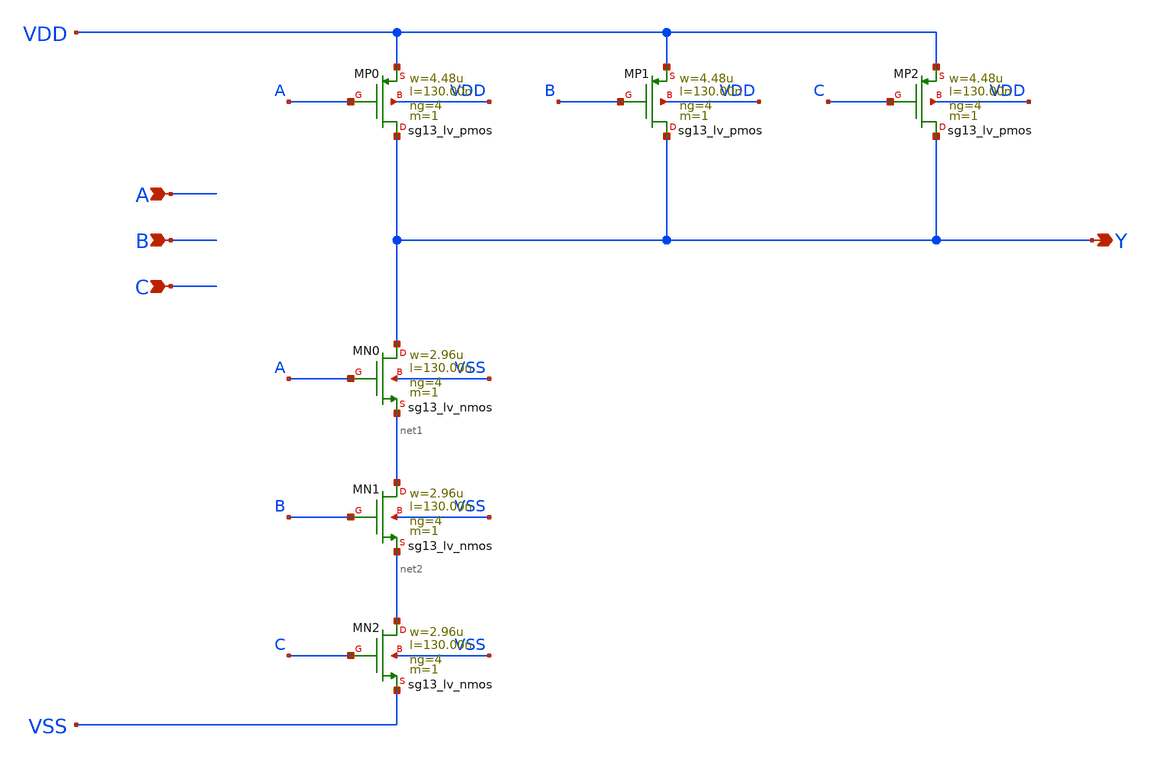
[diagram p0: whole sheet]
** sch_path: outputs/sg13g2_cells/cells/sg13g2_nand3_4/sg13g2_nand3_4.sch
**.subckt sg13g2_nand3_4 A B C Y
*.ipin A
*.ipin B
*.ipin C
*.opin Y
XMN1 net1 B net2 VSS sg13_lv_nmos w=2.96u l=130.00n ng=4 m=1 mm_ok=1
XMN2 net2 C VSS VSS sg13_lv_nmos w=2.96u l=130.00n ng=4 m=1 mm_ok=1
XMN0 Y A net1 VSS sg13_lv_nmos w=2.96u l=130.00n ng=4 m=1 mm_ok=1
XMP0 Y A VDD VDD sg13_lv_pmos w=4.48u l=130.00n ng=4 m=1 mm_ok=1
XMP1 Y B VDD VDD sg13_lv_pmos w=4.48u l=130.00n ng=4 m=1 mm_ok=1
XMP2 Y C VDD VDD sg13_lv_pmos w=4.48u l=130.00n ng=4 m=1 mm_ok=1
**.ends
.end
